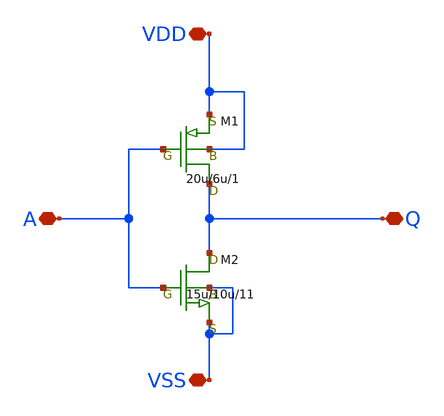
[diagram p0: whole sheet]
** sch_path: member_project/elderline/inverter20241214/inverter.sch
**.subckt inverter Q A VDD VSS
*.iopin Q
*.iopin A
*.iopin VDD
*.iopin VSS
M1 Q A VDD VDD pch w=20u l=6u as=0 ps=0 ad=0 pd=0 m=1
M2 Q A VSS VSS nch w=15u l=10u as=0 ps=0 ad=0 pd=0 m=11
**.ends
.end
